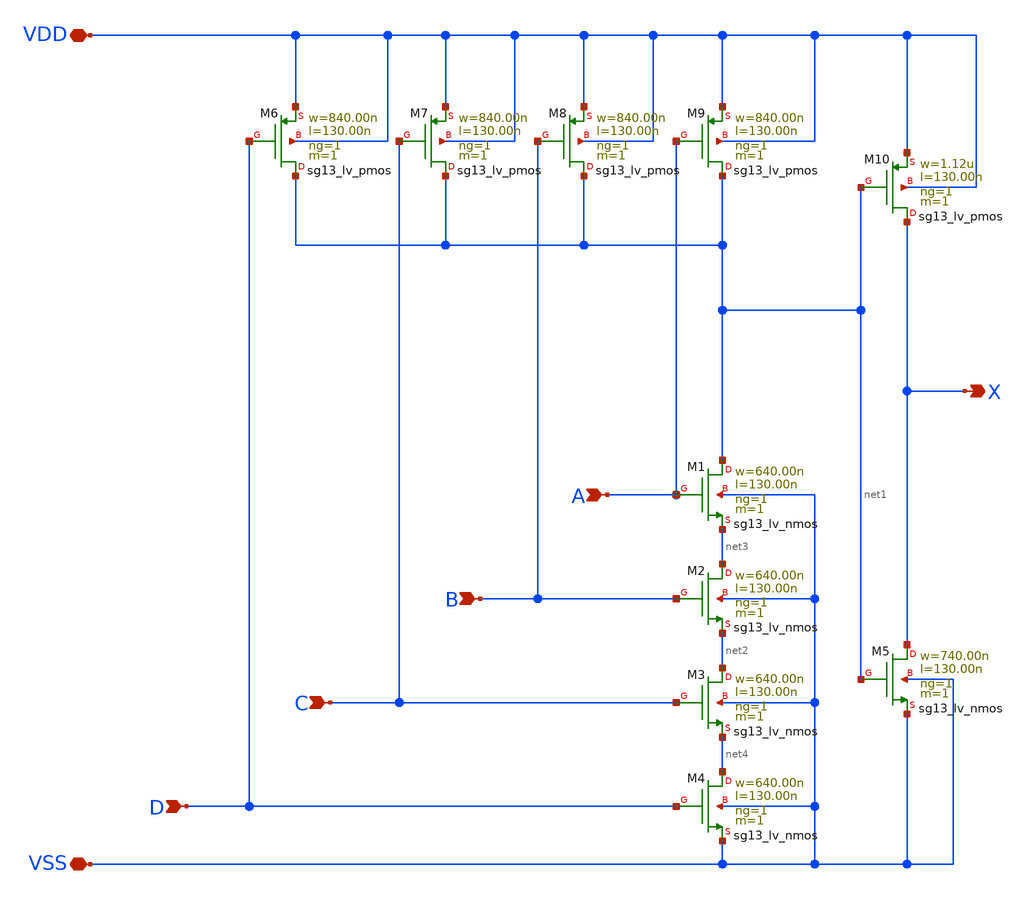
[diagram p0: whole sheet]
** sch_path: ihp-sg13g2/libs.tech/xschem/sg13g2_stdcells/sg13g2_and4_1.sch
* Copyright 2023 IHP PDK Authors
* Licensed under the Apache License, Version 2.0 (the "License");
* you may not use this file except in compliance with the License.
* You may obtain a copy of the License at
* https://www.apache.org/licenses/LICENSE-2.0
* Unless required by applicable law or agreed to in writing, software
* distributed under the License is distributed on an "AS IS" BASIS,
* WITHOUT WARRANTIES OR CONDITIONS OF ANY KIND, either express or implied.
* See the License for the specific language governing permissions and
* limitations under the License.
**.subckt sg13g2_and4_1 A B C D X VDD VSS
*.ipin A
*.ipin B
*.ipin C
*.ipin D
*.opin X
*.iopin VDD
*.iopin VSS
XM1 net1 A net3 VSS sg13_lv_nmos w=640.00n l=130.00n ng=1 m=1 mm_ok=1
XM2 net3 B net2 VSS sg13_lv_nmos w=640.00n l=130.00n ng=1 m=1 mm_ok=1
XM3 net2 C net4 VSS sg13_lv_nmos w=640.00n l=130.00n ng=1 m=1 mm_ok=1
XM4 net4 D VSS VSS sg13_lv_nmos w=640.00n l=130.00n ng=1 m=1 mm_ok=1
XM5 X net1 VSS VSS sg13_lv_nmos w=740.00n l=130.00n ng=1 m=1 mm_ok=1
XM6 net1 D VDD VDD sg13_lv_pmos w=840.00n l=130.00n ng=1 m=1 mm_ok=1
XM7 net1 C VDD VDD sg13_lv_pmos w=840.00n l=130.00n ng=1 m=1 mm_ok=1
XM8 net1 B VDD VDD sg13_lv_pmos w=840.00n l=130.00n ng=1 m=1 mm_ok=1
XM9 net1 A VDD VDD sg13_lv_pmos w=840.00n l=130.00n ng=1 m=1 mm_ok=1
XM10 X net1 VDD VDD sg13_lv_pmos w=1.12u l=130.00n ng=1 m=1 mm_ok=1
**.ends
.end
